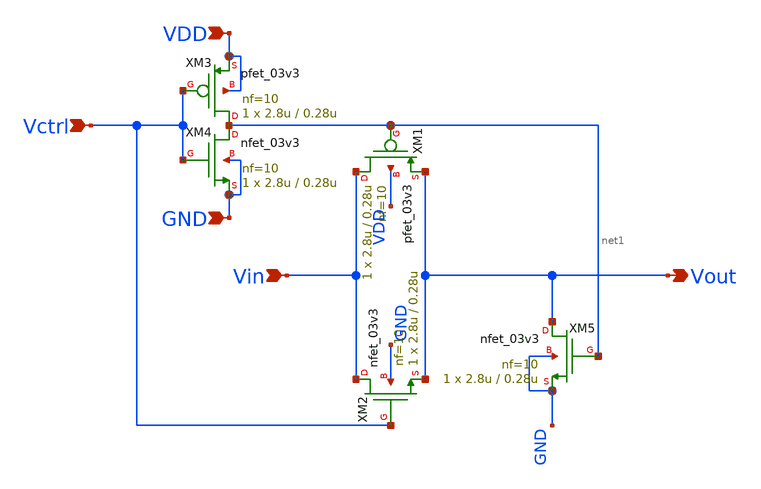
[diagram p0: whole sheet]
** sch_path: maple0705/SAR_ADC/SW_CDAC_NEW.sch
**.subckt SW_CDAC_NEW Vctrl Vin Vout VDD GND
*.ipin Vctrl
*.ipin Vin
*.opin Vout
*.ipin VDD
*.ipin GND
XM1 Vin net1 Vout VDD pfet_03v3 L=0.28u W=2.8u nf=10 ad='int((nf+1)/2) * W/nf * 0.18u' as='int((nf+2)/2) * W/nf * 0.18u'
+ pd='2*int((nf+1)/2) * (W/nf + 0.18u)' ps='2*int((nf+2)/2) * (W/nf + 0.18u)' nrd='0.18u / W' nrs='0.18u / W'
+ sa=0 sb=0 sd=0 m=1
XM2 Vin Vctrl Vout GND nfet_03v3 L=0.28u W=2.8u nf=10 ad='int((nf+1)/2) * W/nf * 0.18u' as='int((nf+2)/2) * W/nf * 0.18u'
+ pd='2*int((nf+1)/2) * (W/nf + 0.18u)' ps='2*int((nf+2)/2) * (W/nf + 0.18u)' nrd='0.18u / W' nrs='0.18u / W'
+ sa=0 sb=0 sd=0 m=1
XM3 net1 Vctrl VDD VDD pfet_03v3 L=0.28u W=2.8u nf=10 ad='int((nf+1)/2) * W/nf * 0.18u' as='int((nf+2)/2) * W/nf * 0.18u'
+ pd='2*int((nf+1)/2) * (W/nf + 0.18u)' ps='2*int((nf+2)/2) * (W/nf + 0.18u)' nrd='0.18u / W' nrs='0.18u / W'
+ sa=0 sb=0 sd=0 m=1
XM4 net1 Vctrl GND GND nfet_03v3 L=0.28u W=2.8u nf=10 ad='int((nf+1)/2) * W/nf * 0.18u' as='int((nf+2)/2) * W/nf * 0.18u'
+ pd='2*int((nf+1)/2) * (W/nf + 0.18u)' ps='2*int((nf+2)/2) * (W/nf + 0.18u)' nrd='0.18u / W' nrs='0.18u / W'
+ sa=0 sb=0 sd=0 m=1
XM5 Vout net1 GND GND nfet_03v3 L=0.28u W=2.8u nf=10 ad='int((nf+1)/2) * W/nf * 0.18u' as='int((nf+2)/2) * W/nf * 0.18u'
+ pd='2*int((nf+1)/2) * (W/nf + 0.18u)' ps='2*int((nf+2)/2) * (W/nf + 0.18u)' nrd='0.18u / W' nrs='0.18u / W'
+ sa=0 sb=0 sd=0 m=1
**.ends
.end
